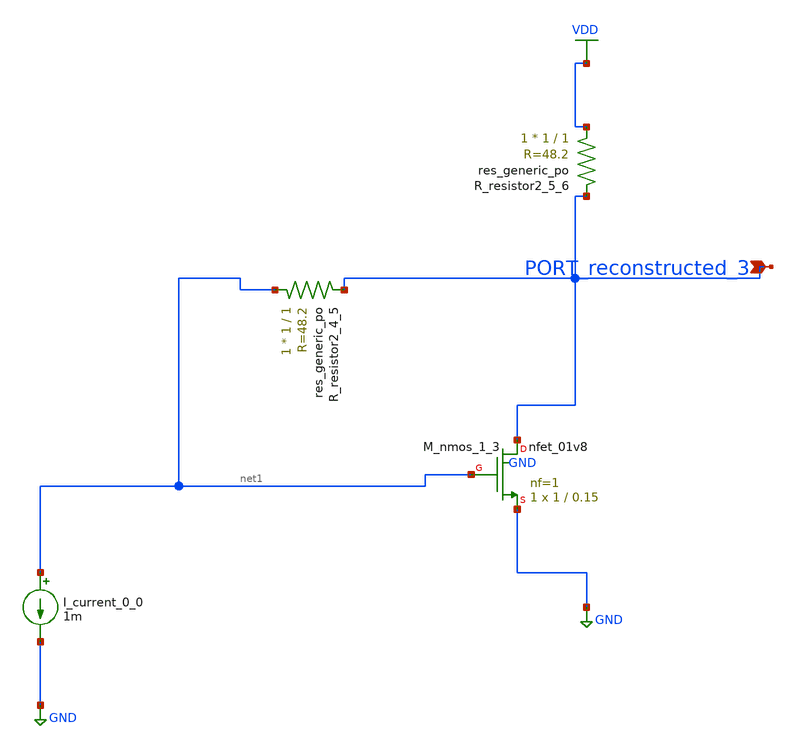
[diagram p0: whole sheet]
** sch_path: schematics/AMSNet/562.sch
**.subckt 562 PORT_reconstructed_3
*.ipin PORT_reconstructed_3
I_current_0_0 net1 GND 1m
XM_nmos_1_3 PORT_reconstructed_3 net1 GND GND sky130_fd_pr__nfet_01v8 L=0.15 W=1 nf=1 ad='int((1 + 1)/2) * 1 / 1 * 0.29'
+ as='int((1 + 2)/2) * 1 / 1 * 0.29' pd='2*int((1 + 1)/2) * (1 / 1 + 0.29)' ps='2*int((1 + 2)/2) * (1 / 1 + 0.29)'
+ nrd='0.29 / 1 ' nrs='0.29 / 1 ' sa=0 sb=0 sd=0 mult=1 m=1
XR_resistor2_4_5 net1 PORT_reconstructed_3 sky130_fd_pr__res_generic_po W=1 L=1 m=1
XR_resistor2_5_6 VDD PORT_reconstructed_3 sky130_fd_pr__res_generic_po W=1 L=1 m=1
**.ends
.GLOBAL GND
.GLOBAL VDD
.end
